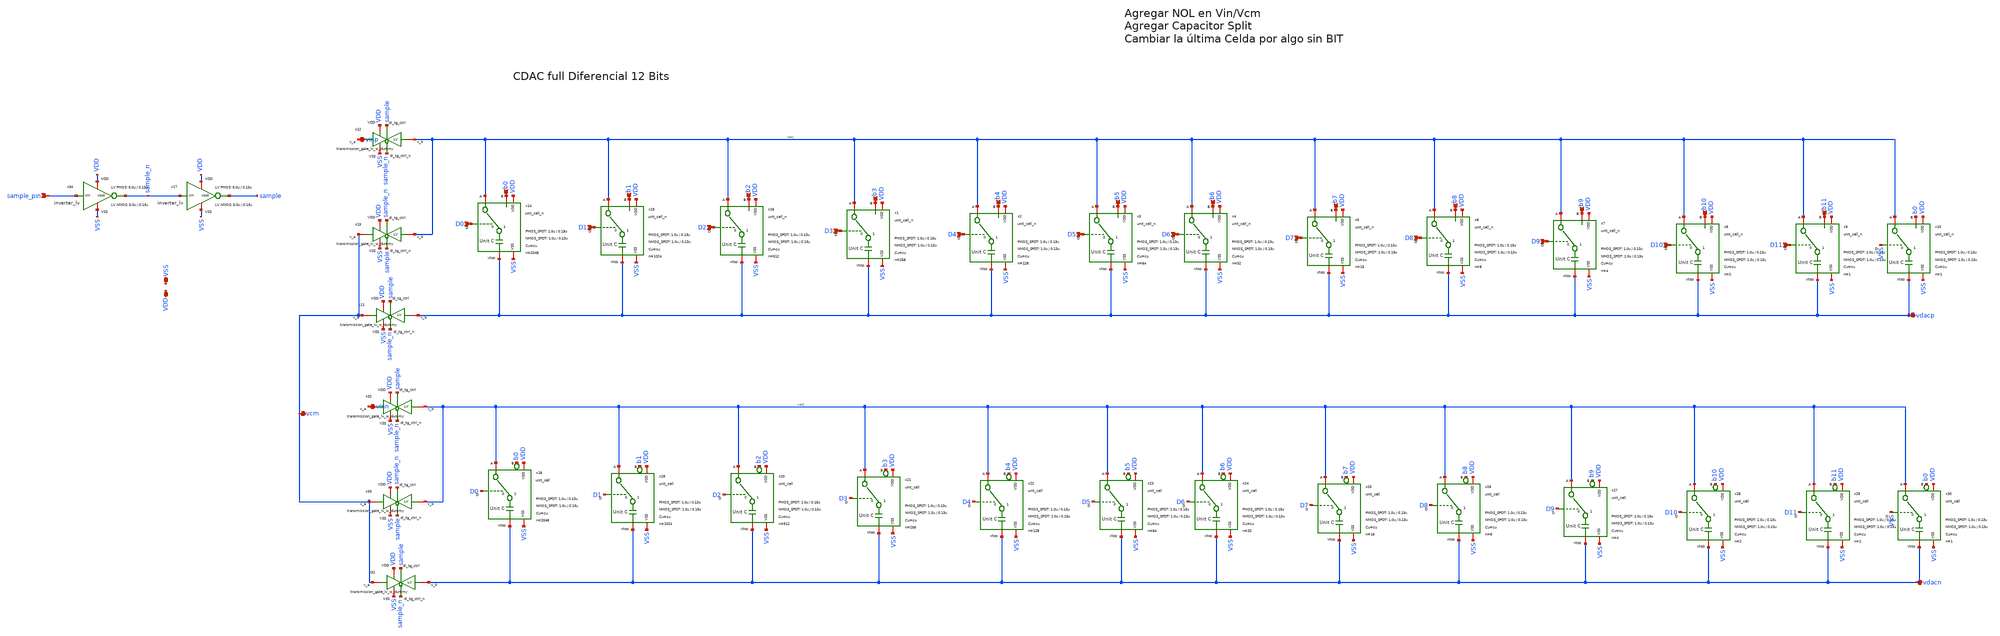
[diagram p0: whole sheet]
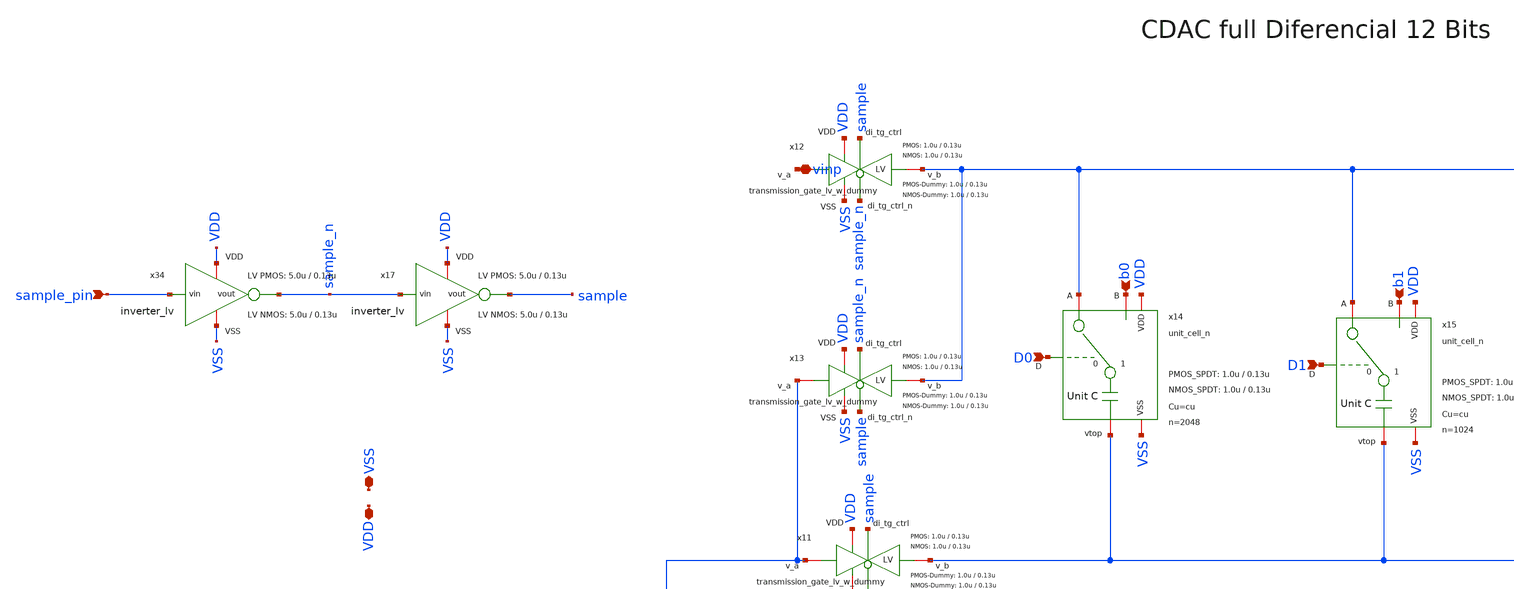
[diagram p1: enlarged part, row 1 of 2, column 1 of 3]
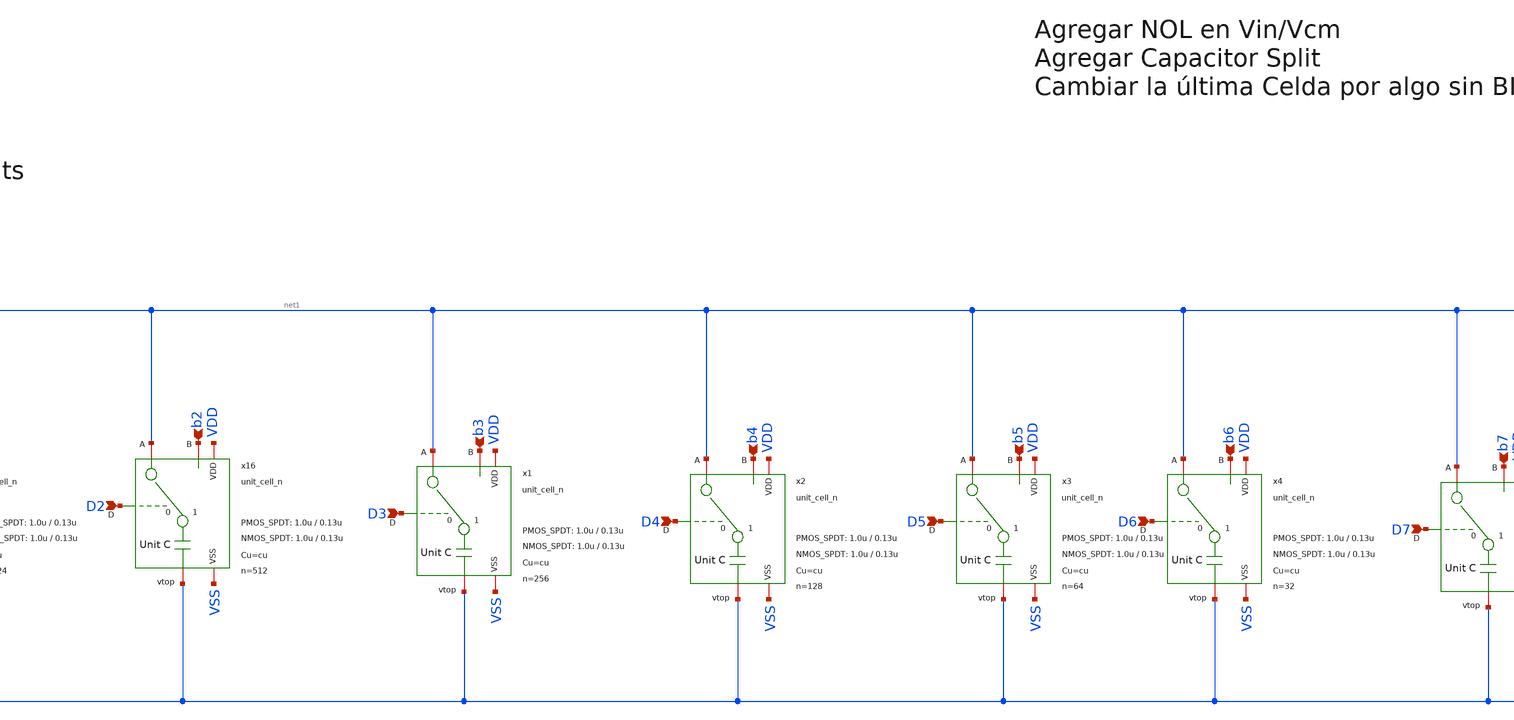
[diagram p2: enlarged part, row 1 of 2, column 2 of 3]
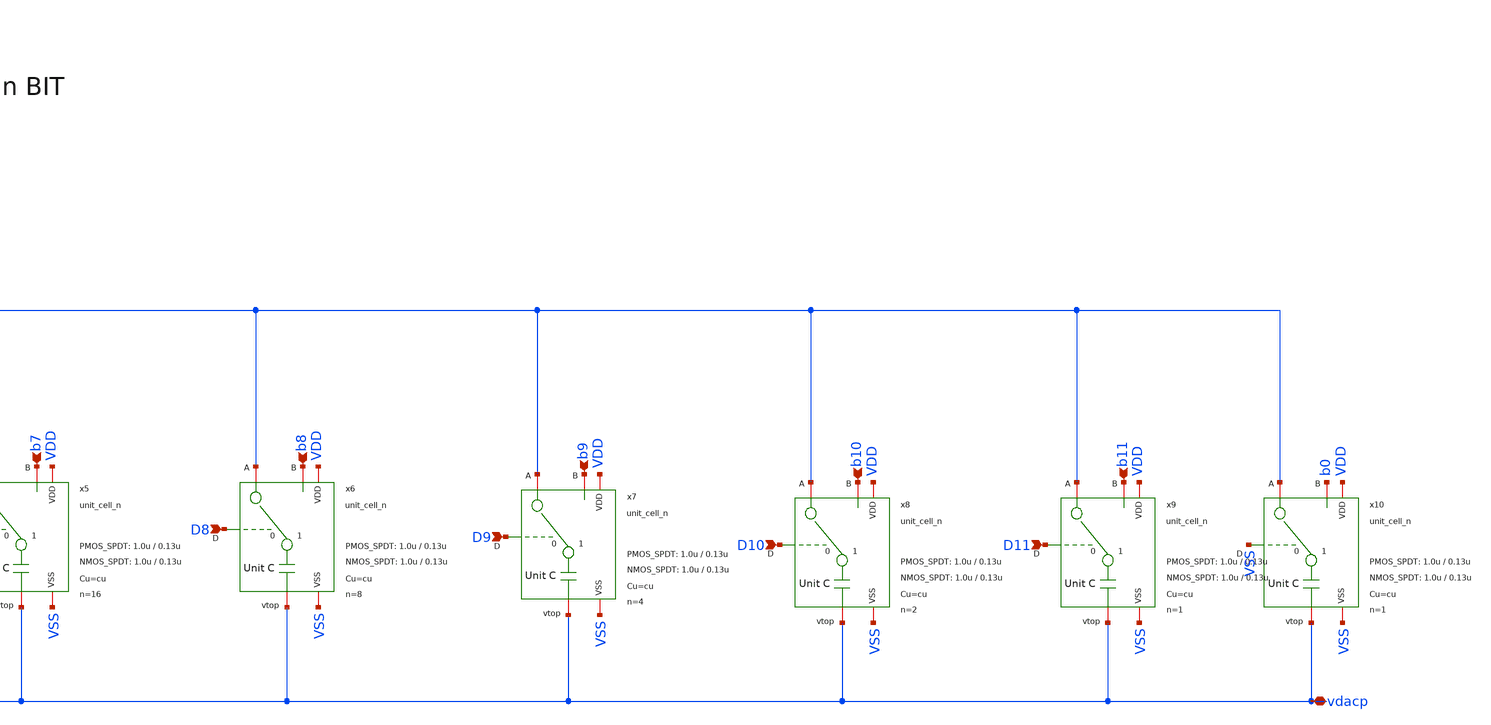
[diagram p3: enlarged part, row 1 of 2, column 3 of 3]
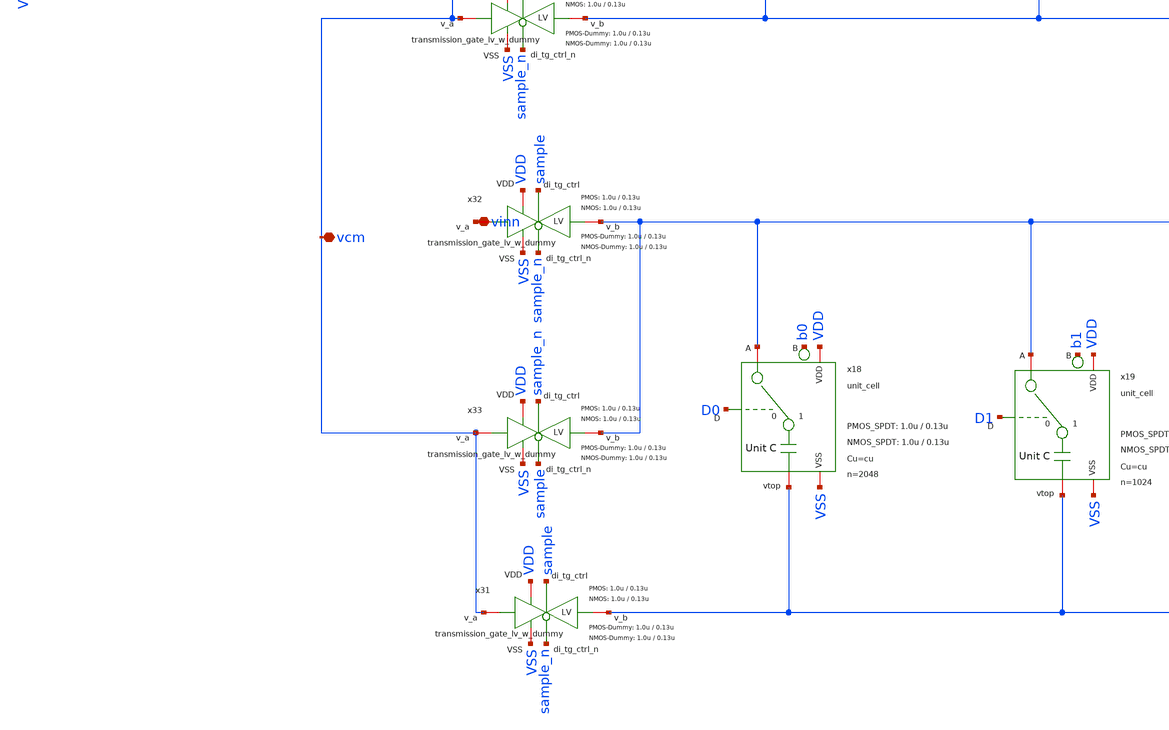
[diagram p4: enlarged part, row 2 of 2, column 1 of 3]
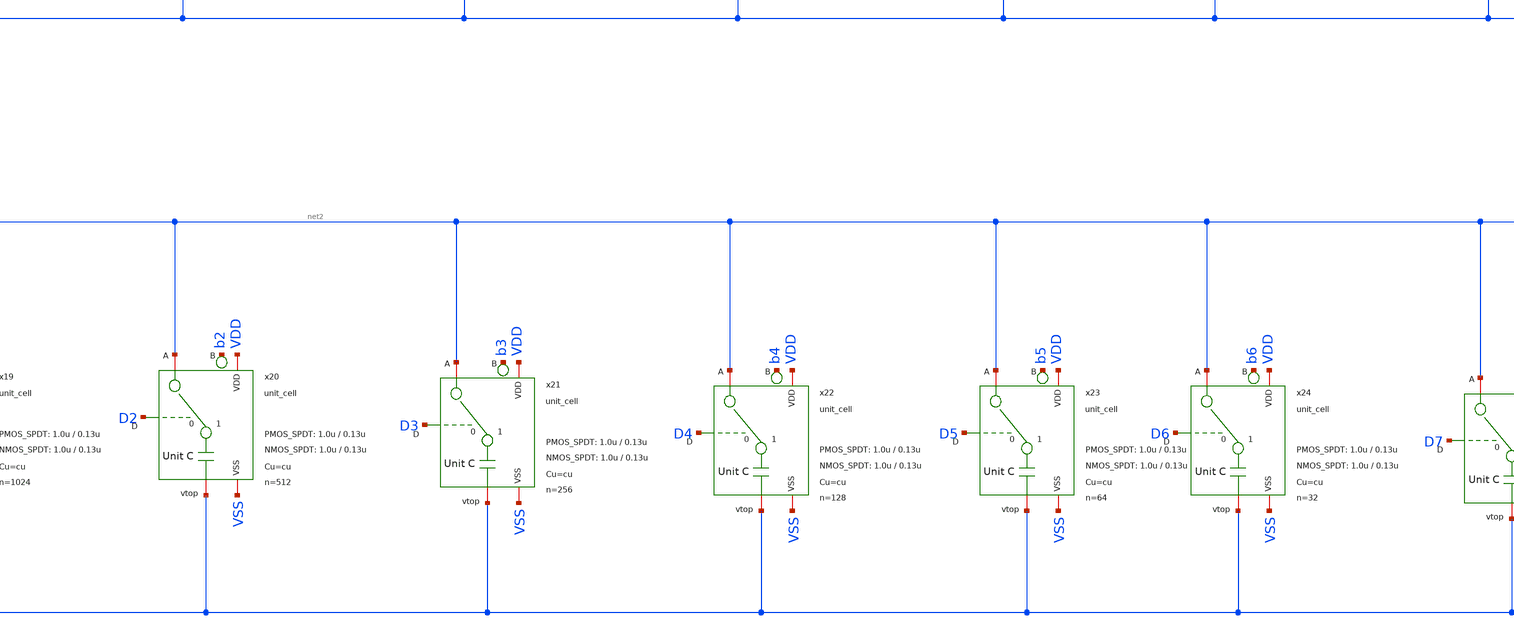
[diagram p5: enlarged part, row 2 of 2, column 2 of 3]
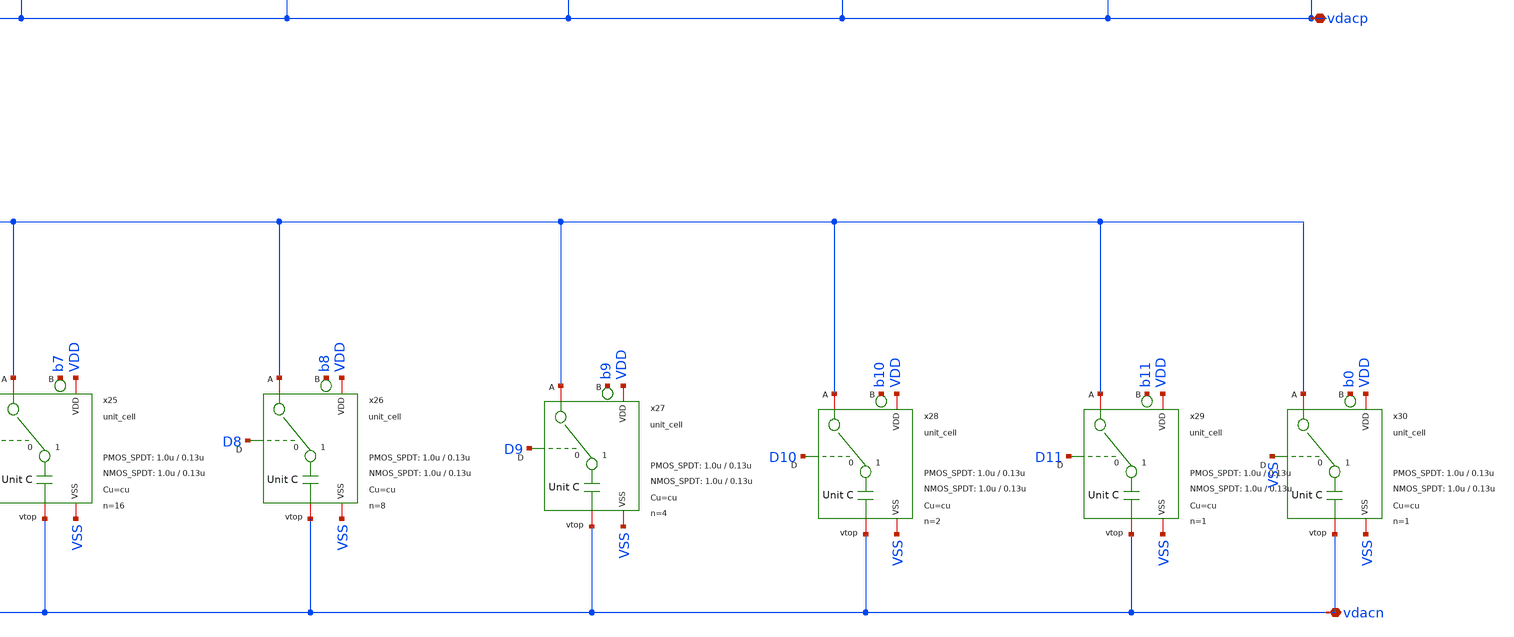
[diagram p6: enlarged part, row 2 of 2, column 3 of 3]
** sch_path: xschem/dac_icms_cell/dac.sch
* IHP-GmbH/IHP-Open-PDK/ihp-sg13g2/libs.tech/xschem/sg13g2_stdcells/sg13g2_dlygate4sd2_1.sch:
* Copyright 2023 IHP PDK Authors
* Licensed under the Apache License, Version 2.0 (the "License");
**.subckt dac D0 b0 D1 b1 D2 b2 D3 b3 D4 b4 D5 b5 D6 b6 D7 b7 D8 b8 D9 b9 D10 b10 D11 b11 vinp vcm
*+ sample_pin vinn vdacp vdacn VSS VDD
*.ipin D0
*.ipin b0
*.ipin D1
*.ipin b1
*.ipin D2
*.ipin b2
*.ipin D3
*.ipin b3
*.ipin D4
*.ipin b4
*.ipin D5
*.ipin b5
*.ipin D6
*.ipin b6
*.ipin D7
*.ipin b7
*.ipin D8
*.ipin b8
*.ipin D9
*.ipin b9
*.ipin D10
*.ipin b10
*.ipin D11
*.ipin b11
*.iopin vinp
*.iopin vcm
*.ipin sample_pin
*.iopin vinn
*.iopin vdacp
*.iopin vdacn
*.iopin VSS
*.iopin VDD
x14 b0 net1 VSS D0 VDD vdacp unit_cell_n W_P_SPDT=1.0u L_P_SPDT=0.13u W_N_SPDT=1.0u L_N_SPDT=0.13u
+ Cu=cu n=2048
x15 b1 net1 VSS D1 VDD vdacp unit_cell_n W_P_SPDT=1.0u L_P_SPDT=0.13u W_N_SPDT=1.0u L_N_SPDT=0.13u
+ Cu=cu n=1024
x16 b2 net1 VSS D2 VDD vdacp unit_cell_n W_P_SPDT=1.0u L_P_SPDT=0.13u W_N_SPDT=1.0u L_N_SPDT=0.13u
+ Cu=cu n=512
x1 b3 net1 VSS D3 VDD vdacp unit_cell_n W_P_SPDT=1.0u L_P_SPDT=0.13u W_N_SPDT=1.0u L_N_SPDT=0.13u
+ Cu=cu n=256
x2 b4 net1 VSS D4 VDD vdacp unit_cell_n W_P_SPDT=1.0u L_P_SPDT=0.13u W_N_SPDT=1.0u L_N_SPDT=0.13u
+ Cu=cu n=128
x3 b5 net1 VSS D5 VDD vdacp unit_cell_n W_P_SPDT=1.0u L_P_SPDT=0.13u W_N_SPDT=1.0u L_N_SPDT=0.13u
+ Cu=cu n=64
x4 b6 net1 VSS D6 VDD vdacp unit_cell_n W_P_SPDT=1.0u L_P_SPDT=0.13u W_N_SPDT=1.0u L_N_SPDT=0.13u
+ Cu=cu n=32
x5 b7 net1 VSS D7 VDD vdacp unit_cell_n W_P_SPDT=1.0u L_P_SPDT=0.13u W_N_SPDT=1.0u L_N_SPDT=0.13u
+ Cu=cu n=16
x6 b8 net1 VSS D8 VDD vdacp unit_cell_n W_P_SPDT=1.0u L_P_SPDT=0.13u W_N_SPDT=1.0u L_N_SPDT=0.13u
+ Cu=cu n=8
x7 b9 net1 VSS D9 VDD vdacp unit_cell_n W_P_SPDT=1.0u L_P_SPDT=0.13u W_N_SPDT=1.0u L_N_SPDT=0.13u
+ Cu=cu n=4
x8 b10 net1 VSS D10 VDD vdacp unit_cell_n W_P_SPDT=1.0u L_P_SPDT=0.13u W_N_SPDT=1.0u L_N_SPDT=0.13u
+ Cu=cu n=2
x9 b11 net1 VSS D11 VDD vdacp unit_cell_n W_P_SPDT=1.0u L_P_SPDT=0.13u W_N_SPDT=1.0u L_N_SPDT=0.13u
+ Cu=cu n=1
x10 b0 net1 VSS VSS VDD vdacp unit_cell_n W_P_SPDT=1.0u L_P_SPDT=0.13u W_N_SPDT=1.0u L_N_SPDT=0.13u
+ Cu=cu n=1
x11 VDD sample VSS vdacp vcm sample_n transmission_gate_lv_w_dummy W_P=1.0u L_P=0.13u W_N=1.0u
+ L_N=0.13u W_P_D=1.0u L_P_D=0.13u W_N_D=1.0u L_N_D=0.13u n=10
x12 VDD sample VSS net1 vinp sample_n transmission_gate_lv_w_dummy W_P=1.0u L_P=0.13u W_N=1.0u
+ L_N=0.13u W_P_D=1.0u L_P_D=0.13u W_N_D=1.0u L_N_D=0.13u n=10
x13 VDD sample_n VSS net1 vcm sample transmission_gate_lv_w_dummy W_P=1.0u L_P=0.13u W_N=1.0u
+ L_N=0.13u W_P_D=1.0u L_P_D=0.13u W_N_D=1.0u L_N_D=0.13u n=10
x17 VDD sample_n sample VSS inverter_lv W_P=5.0u L_P=0.13u W_N=5.0u L_N=0.13u n=10
x18 b0 net2 VSS D0 VDD vdacn unit_cell W_P_SPDT=1.0u L_P_SPDT=0.13u W_N_SPDT=1.0u L_N_SPDT=0.13u
+ Cu=cu n=2048
x19 b1 net2 VSS D1 VDD vdacn unit_cell W_P_SPDT=1.0u L_P_SPDT=0.13u W_N_SPDT=1.0u L_N_SPDT=0.13u
+ Cu=cu n=1024
x20 b2 net2 VSS D2 VDD vdacn unit_cell W_P_SPDT=1.0u L_P_SPDT=0.13u W_N_SPDT=1.0u L_N_SPDT=0.13u
+ Cu=cu n=512
x21 b3 net2 VSS D3 VDD vdacn unit_cell W_P_SPDT=1.0u L_P_SPDT=0.13u W_N_SPDT=1.0u L_N_SPDT=0.13u
+ Cu=cu n=256
x22 b4 net2 VSS D4 VDD vdacn unit_cell W_P_SPDT=1.0u L_P_SPDT=0.13u W_N_SPDT=1.0u L_N_SPDT=0.13u
+ Cu=cu n=128
x23 b5 net2 VSS D5 VDD vdacn unit_cell W_P_SPDT=1.0u L_P_SPDT=0.13u W_N_SPDT=1.0u L_N_SPDT=0.13u
+ Cu=cu n=64
x24 b6 net2 VSS D6 VDD vdacn unit_cell W_P_SPDT=1.0u L_P_SPDT=0.13u W_N_SPDT=1.0u L_N_SPDT=0.13u
+ Cu=cu n=32
x25 b7 net2 VSS D7 VDD vdacn unit_cell W_P_SPDT=1.0u L_P_SPDT=0.13u W_N_SPDT=1.0u L_N_SPDT=0.13u
+ Cu=cu n=16
x26 b8 net2 VSS D8 VDD vdacn unit_cell W_P_SPDT=1.0u L_P_SPDT=0.13u W_N_SPDT=1.0u L_N_SPDT=0.13u
+ Cu=cu n=8
x27 b9 net2 VSS D9 VDD vdacn unit_cell W_P_SPDT=1.0u L_P_SPDT=0.13u W_N_SPDT=1.0u L_N_SPDT=0.13u
+ Cu=cu n=4
x28 b10 net2 VSS D10 VDD vdacn unit_cell W_P_SPDT=1.0u L_P_SPDT=0.13u W_N_SPDT=1.0u L_N_SPDT=0.13u
+ Cu=cu n=2
x29 b11 net2 VSS D11 VDD vdacn unit_cell W_P_SPDT=1.0u L_P_SPDT=0.13u W_N_SPDT=1.0u L_N_SPDT=0.13u
+ Cu=cu n=1
x30 b0 net2 VSS VSS VDD vdacn unit_cell W_P_SPDT=1.0u L_P_SPDT=0.13u W_N_SPDT=1.0u L_N_SPDT=0.13u
+ Cu=cu n=1
x31 VDD sample VSS vdacn vcm sample_n transmission_gate_lv_w_dummy W_P=1.0u L_P=0.13u W_N=1.0u
+ L_N=0.13u W_P_D=1.0u L_P_D=0.13u W_N_D=1.0u L_N_D=0.13u n=10
x32 VDD sample VSS net2 vinn sample_n transmission_gate_lv_w_dummy W_P=1.0u L_P=0.13u W_N=1.0u
+ L_N=0.13u W_P_D=1.0u L_P_D=0.13u W_N_D=1.0u L_N_D=0.13u n=10
x33 VDD sample_n VSS net2 vcm sample transmission_gate_lv_w_dummy W_P=1.0u L_P=0.13u W_N=1.0u
+ L_N=0.13u W_P_D=1.0u L_P_D=0.13u W_N_D=1.0u L_N_D=0.13u n=10
x34 VDD sample_pin sample_n VSS inverter_lv W_P=5.0u L_P=0.13u W_N=5.0u L_N=0.13u n=10
**.ends

* expanding   symbol:  dac_icms_cell/unit_cell_n.sym # of pins=6
** sym_path: xschem/dac_icms_cell/unit_cell_n.sym
** sch_path: xschem/dac_icms_cell/unit_cell_n.sch
.subckt unit_cell_n B A VSS D VDD vtop  W_P_SPDT=1.0u L_P_SPDT=0.13u W_N_SPDT=1.0u L_N_SPDT=0.13u
+ Cu=8f n=1
*.iopin VSS
*.iopin A
*.iopin VDD
*.ipin D
*.iopin B
*.iopin vtop
x1 VDD net3 VSS net1 net2 A dac_switch_n W_P_TG=3.0u L_P_TG=0.13u W_N_TG=1.0u L_N_TG=0.13u n={1}
C1 net1 vtop cu m=n
x35 VDD B net2 VSS buffer_lv W_P_INV=10.0u L_P_INV=0.13u W_N_INV=10.0u L_N_INV=0.13u
x2 VDD D net3 VSS buffer_lv W_P_INV=10.0u L_P_INV=0.13u W_N_INV=10.0u L_N_INV=0.13u
.ends


* expanding   symbol:  transmission_gate/transmission_gate_lv_w_dummy.sym # of pins=6
** sym_path: xschem/transmission_gate/transmission_gate_lv_w_dummy.sym
** sch_path: xschem/transmission_gate/transmission_gate_lv_w_dummy.sch
.subckt transmission_gate_lv_w_dummy VDD di_tg_ctrl VSS v_b v_a di_tg_ctrl_n  W_P=2.0u L_P=0.13u
+ W_N=2.0u L_N=0.13u W_P_D=1.0u L_P_D=0.13u W_N_D=1.0u L_N_D=0.13u n=1
*.iopin v_a
*.iopin v_b
*.iopin VDD
*.iopin VSS
*.ipin di_tg_ctrl
*.ipin di_tg_ctrl_n
XM1 v_a di_tg_ctrl v_b VSS sg13_lv_nmos w=W_N l=L_N ng=1 m=n mm_ok=1
XM2 v_a di_tg_ctrl_n v_b VDD sg13_lv_pmos w=W_P l=L_P ng=1 m=n mm_ok=1
XMdummy2 v_b di_tg_ctrl v_b VDD sg13_lv_pmos w=W_P_D l=L_P_D ng=1 m=n mm_ok=1
XMdummy1 v_b di_tg_ctrl_n v_b VSS sg13_lv_nmos w=W_N_D l=L_N_D ng=1 m=n mm_ok=1
.ends


* expanding   symbol:  inverter/inverter_lv.sym # of pins=4
** sym_path: xschem/inverter/inverter_lv.sym
** sch_path: xschem/inverter/inverter_lv.sch
.subckt inverter_lv VDD vin vout VSS  W_P=3.0u L_P=0.13u W_N=1.0u L_N=0.13u n=1
*.ipin vin
*.iopin VDD
*.iopin VSS
*.opin vout
XM1 vout vin VDD VDD sg13_lv_pmos w=W_P l=L_P ng=1 m=n mm_ok=1
XM2 vout vin VSS VSS sg13_lv_nmos w=W_N l=L_N ng=1 m=n mm_ok=1
.ends


* expanding   symbol:  dac_icms_cell/unit_cell.sym # of pins=6
** sym_path: xschem/dac_icms_cell/unit_cell.sym
** sch_path: xschem/dac_icms_cell/unit_cell.sch
.subckt unit_cell B A VSS D VDD vtop  W_P_SPDT=1.0u L_P_SPDT=0.13u W_N_SPDT=1.0u L_N_SPDT=0.13u
+ Cu=8f n=1
*.iopin VSS
*.iopin A
*.iopin VDD
*.ipin D
*.iopin B
*.iopin vtop
x1 VDD net3 VSS net1 net2 A dac_switch W_P_TG=3.0u L_P_TG=0.13u W_N_TG=1.0u L_N_TG=0.13u n={1}
C1 net1 vtop Cu m=n
x35 VDD B net2 VSS buffer_lv W_P_INV=10.0u L_P_INV=0.13u W_N_INV=10.0u L_N_INV=0.13u
x2 VDD D net3 VSS buffer_lv W_P_INV=10.0u L_P_INV=0.13u W_N_INV=10.0u L_N_INV=0.13u
.ends


* expanding   symbol:  dac_icms_cell/dac_switch_n.sym # of pins=6
** sym_path: xschem/dac_icms_cell/dac_switch_n.sym
** sch_path: xschem/dac_icms_cell/dac_switch_n.sch
.subckt dac_switch_n VDD di_spdt_ctrl VSS v_c v_b v_a  W_P_TG=3.0u L_P_TG=0.13u W_N_TG=1.0u
+ L_N_TG=0.13u n=1
*.iopin v_a
*.iopin v_c
*.iopin VDD
*.iopin VSS
*.ipin di_spdt_ctrl
*.iopin v_b
x1 VDD di_spdt_ctrl VSS v_c v_a di_spdt_ctrl_n transmission_gate_lv_wo_dummy W_P=W_P_TG L_P=L_P_TG
+ W_N=W_N_TG L_N=L_N_TG W_P_D=1.0u L_P_D=0.13u W_N_D=1.0u L_N_D=0.13u n=n
x8 VDD di_spdt_ctrl di_spdt_ctrl_n VSS inverter_lv W_P=W_P_TG L_P=L_P_TG W_N=W_N_TG L_N=L_N_TG n=n
XM1 net1 net2 VSS VSS sg13_lv_nmos w=0.5u l=0.2u ng=1 m=n mm_ok=1
XM3 net1 net2 VDD VDD sg13_lv_pmos w=1u l=0.2u ng=1 m=n mm_ok=1
x2 VDD net3 VSS net1 v_c net4 transmission_gate_lv_w_dummy W_P=W_P_TG L_P=L_P_TG W_N=W_N_TG
+ L_N=L_N_TG W_P_D=1.0u L_P_D=0.13u W_N_D=1.0u L_N_D=0.13u n=n
XM2 net2 v_b VSS VSS sg13_lv_nmos w=0.5u l=0.2u ng=1 m=n mm_ok=1
XM4 net2 v_b VDD VDD sg13_lv_pmos w=1u l=0.2u ng=1 m=n mm_ok=1
x40 net3 di_spdt_ctrl_n VDD VSS sg13g2_dlygate4sd2_1
x3 net4 di_spdt_ctrl VDD VSS sg13g2_dlygate4sd2_1
.ends


* expanding   symbol:  buffer/buffer_lv.sym # of pins=4
** sym_path: buffer/buffer_lv.sym
** sch_path: buffer/buffer_lv.sch
.subckt buffer_lv VDD vin vout VSS  W_P_INV=3.0u L_P_INV=0.13u W_N_INV=1.0u L_N_INV=0.13u
*.ipin vin
*.iopin VDD
*.iopin VSS
*.opin vout
x1 VDD vin net1 VSS inverter_lv W_P=W_P_INV L_P=L_P_INV W_N=W_N_INV L_N=L_N_INV n=1
x2 VDD net1 vout VSS inverter_lv W_P=W_P_INV L_P=L_P_INV W_N=W_N_INV L_N=L_N_INV n=1
.ends


* expanding   symbol:  dac_icms_cell/dac_switch.sym # of pins=6
** sym_path: xschem/dac_icms_cell/dac_switch.sym
** sch_path: xschem/dac_icms_cell/dac_switch.sch
.subckt dac_switch VDD di_spdt_ctrl VSS v_c v_b v_a  W_P_TG=3.0u L_P_TG=0.13u W_N_TG=1.0u
+ L_N_TG=0.13u n=1
*.iopin v_a
*.iopin v_c
*.iopin VDD
*.iopin VSS
*.ipin di_spdt_ctrl
*.iopin v_b
x1 VDD di_spdt_ctrl VSS v_c v_a di_spdt_ctrl_n transmission_gate_lv_w_dummy W_P=W_P_TG L_P=L_P_TG
+ W_N=W_N_TG L_N=L_N_TG W_P_D=1.0u L_P_D=0.13u W_N_D=1.0u L_N_D=0.13u n=n
x8 VDD di_spdt_ctrl di_spdt_ctrl_n VSS inverter_lv W_P=W_P_TG L_P=L_P_TG W_N=W_N_TG L_N=L_N_TG n=1
XM1 net1 v_b VSS VSS sg13_lv_nmos w=0.5u l=0.2u ng=1 m=n mm_ok=1
XM3 net1 v_b VDD VDD sg13_lv_pmos w=1u l=0.2u ng=1 m=n mm_ok=1
x2 VDD net2 VSS net1 v_c net3 transmission_gate_lv_w_dummy W_P=W_P_TG L_P=L_P_TG W_N=W_N_TG
+ L_N=L_N_TG W_P_D=1.0u L_P_D=0.13u W_N_D=1.0u L_N_D=0.13u n=n
x40 net2 di_spdt_ctrl_n VDD VSS sg13g2_dlygate4sd2_1
x4 net3 di_spdt_ctrl VDD VSS sg13g2_dlygate4sd2_1
.ends


* expanding   symbol:  transmission_gate/transmission_gate_lv_wo_dummy.sym # of pins=6
** sym_path: xschem/transmission_gate/transmission_gate_lv_wo_dummy.sym
** sch_path: xschem/transmission_gate/transmission_gate_lv_wo_dummy.sch
.subckt transmission_gate_lv_wo_dummy VDD di_tg_ctrl VSS v_b v_a di_tg_ctrl_n  W_P=2.0u L_P=0.13u
+ W_N=2.0u L_N=0.13u W_P_D=1.0u L_P_D=0.13u W_N_D=1.0u L_N_D=0.13u n=1
*.iopin v_a
*.iopin v_b
*.iopin VDD
*.iopin VSS
*.ipin di_tg_ctrl
*.ipin di_tg_ctrl_n
XM1 v_a di_tg_ctrl v_b VSS sg13_lv_nmos w=W_N l=L_N ng=1 m=n mm_ok=1
XM2 v_a di_tg_ctrl_n v_b VDD sg13_lv_pmos w=W_P l=L_P ng=1 m=n mm_ok=1
.ends


* expanding   symbol:  sg13g2_stdcells/sg13g2_dlygate4sd2_1.sym # of pins=2
** sym_path: sg13g2_stdcells/sg13g2_dlygate4sd2_1.sym
** sch_path: sg13g2_stdcells/sg13g2_dlygate4sd2_1.sch
.subckt sg13g2_dlygate4sd2_1 X A VDD VSS
*.ipin A
*.opin X
*.iopin VDD
*.iopin VSS
XM1 net2 A VSS VSS sg13_lv_nmos w=420.00n l=130.00n ng=1 m=1 mm_ok=1
XM2 net1 net2 VSS VSS sg13_lv_nmos w=420.00n l=180.00n ng=1 m=1 mm_ok=1
XM3 net3 net1 VSS VSS sg13_lv_nmos w=420.00n l=180.00n ng=1 m=1 mm_ok=1
XM4 X net3 VSS VSS sg13_lv_nmos w=740.00n l=130.00n ng=1 m=1 mm_ok=1
XM5 net2 A VDD VDD sg13_lv_pmos w=420.00n l=130.00n ng=1 m=1 mm_ok=1
XM6 net1 net2 VDD VDD sg13_lv_pmos w=1.000u l=250.00n ng=1 m=1 mm_ok=1
XM7 net3 net1 VDD VDD sg13_lv_pmos w=1.000u l=250.00n ng=1 m=1 mm_ok=1
XM8 X net3 VDD VDD sg13_lv_pmos w=1.12u l=130.00n ng=1 m=1 mm_ok=1
.ends

.end
